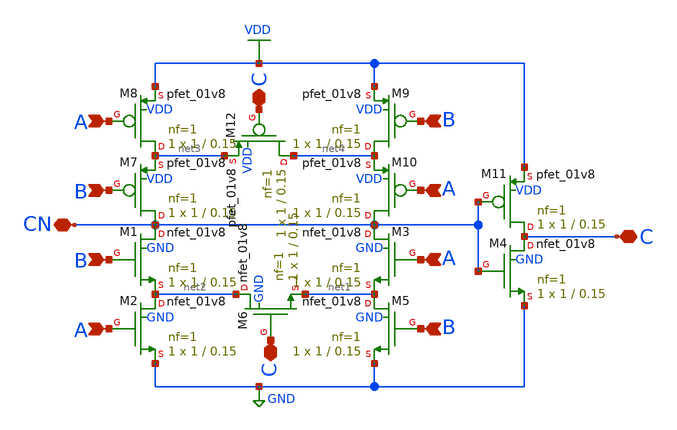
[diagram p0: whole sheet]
** sch_path: cells/xschem/ASYNC3.sch
**.subckt ASYNC3 A B B A B A A B C C CN C
*.ipin A
*.ipin B
*.ipin B
*.ipin A
*.ipin B
*.ipin A
*.ipin A
*.ipin B
*.iopin C
*.iopin C
*.iopin CN
*.iopin C
XM1 CN B net2 GND sky130_fd_pr__nfet_01v8 L=0.15 W=1 nf=1 ad='int((nf+1)/2) * W/nf * 0.29' as='int((nf+2)/2) * W/nf * 0.29'
+ pd='2*int((nf+1)/2) * (W/nf + 0.29)' ps='2*int((nf+2)/2) * (W/nf + 0.29)' nrd='0.29 / W' nrs='0.29 / W'
+ sa=0 sb=0 sd=0 mult=1 m=1
XM2 net2 A GND GND sky130_fd_pr__nfet_01v8 L=0.15 W=1 nf=1 ad='int((nf+1)/2) * W/nf * 0.29' as='int((nf+2)/2) * W/nf * 0.29'
+ pd='2*int((nf+1)/2) * (W/nf + 0.29)' ps='2*int((nf+2)/2) * (W/nf + 0.29)' nrd='0.29 / W' nrs='0.29 / W'
+ sa=0 sb=0 sd=0 mult=1 m=1
XM3 CN A net1 GND sky130_fd_pr__nfet_01v8 L=0.15 W=1 nf=1 ad='int((nf+1)/2) * W/nf * 0.29' as='int((nf+2)/2) * W/nf * 0.29'
+ pd='2*int((nf+1)/2) * (W/nf + 0.29)' ps='2*int((nf+2)/2) * (W/nf + 0.29)' nrd='0.29 / W' nrs='0.29 / W'
+ sa=0 sb=0 sd=0 mult=1 m=1
XM4 C CN GND GND sky130_fd_pr__nfet_01v8 L=0.15 W=1 nf=1 ad='int((nf+1)/2) * W/nf * 0.29' as='int((nf+2)/2) * W/nf * 0.29'
+ pd='2*int((nf+1)/2) * (W/nf + 0.29)' ps='2*int((nf+2)/2) * (W/nf + 0.29)' nrd='0.29 / W' nrs='0.29 / W'
+ sa=0 sb=0 sd=0 mult=1 m=1
XM5 net1 B GND GND sky130_fd_pr__nfet_01v8 L=0.15 W=1 nf=1 ad='int((nf+1)/2) * W/nf * 0.29' as='int((nf+2)/2) * W/nf * 0.29'
+ pd='2*int((nf+1)/2) * (W/nf + 0.29)' ps='2*int((nf+2)/2) * (W/nf + 0.29)' nrd='0.29 / W' nrs='0.29 / W'
+ sa=0 sb=0 sd=0 mult=1 m=1
XM6 net2 C net1 GND sky130_fd_pr__nfet_01v8 L=0.15 W=1 nf=1 ad='int((nf+1)/2) * W/nf * 0.29' as='int((nf+2)/2) * W/nf * 0.29'
+ pd='2*int((nf+1)/2) * (W/nf + 0.29)' ps='2*int((nf+2)/2) * (W/nf + 0.29)' nrd='0.29 / W' nrs='0.29 / W'
+ sa=0 sb=0 sd=0 mult=1 m=1
XM7 CN B net3 VDD sky130_fd_pr__pfet_01v8 L=0.15 W=1 nf=1 ad='int((nf+1)/2) * W/nf * 0.29' as='int((nf+2)/2) * W/nf * 0.29'
+ pd='2*int((nf+1)/2) * (W/nf + 0.29)' ps='2*int((nf+2)/2) * (W/nf + 0.29)' nrd='0.29 / W' nrs='0.29 / W'
+ sa=0 sb=0 sd=0 mult=1 m=1
XM8 net3 A VDD VDD sky130_fd_pr__pfet_01v8 L=0.15 W=1 nf=1 ad='int((nf+1)/2) * W/nf * 0.29' as='int((nf+2)/2) * W/nf * 0.29'
+ pd='2*int((nf+1)/2) * (W/nf + 0.29)' ps='2*int((nf+2)/2) * (W/nf + 0.29)' nrd='0.29 / W' nrs='0.29 / W'
+ sa=0 sb=0 sd=0 mult=1 m=1
XM9 net4 B VDD VDD sky130_fd_pr__pfet_01v8 L=0.15 W=1 nf=1 ad='int((nf+1)/2) * W/nf * 0.29' as='int((nf+2)/2) * W/nf * 0.29'
+ pd='2*int((nf+1)/2) * (W/nf + 0.29)' ps='2*int((nf+2)/2) * (W/nf + 0.29)' nrd='0.29 / W' nrs='0.29 / W'
+ sa=0 sb=0 sd=0 mult=1 m=1
XM10 CN A net4 VDD sky130_fd_pr__pfet_01v8 L=0.15 W=1 nf=1 ad='int((nf+1)/2) * W/nf * 0.29' as='int((nf+2)/2) * W/nf * 0.29'
+ pd='2*int((nf+1)/2) * (W/nf + 0.29)' ps='2*int((nf+2)/2) * (W/nf + 0.29)' nrd='0.29 / W' nrs='0.29 / W'
+ sa=0 sb=0 sd=0 mult=1 m=1
XM11 C CN VDD VDD sky130_fd_pr__pfet_01v8 L=0.15 W=1 nf=1 ad='int((nf+1)/2) * W/nf * 0.29' as='int((nf+2)/2) * W/nf * 0.29'
+ pd='2*int((nf+1)/2) * (W/nf + 0.29)' ps='2*int((nf+2)/2) * (W/nf + 0.29)' nrd='0.29 / W' nrs='0.29 / W'
+ sa=0 sb=0 sd=0 mult=1 m=1
XM12 net4 C net3 VDD sky130_fd_pr__pfet_01v8 L=0.15 W=1 nf=1 ad='int((nf+1)/2) * W/nf * 0.29' as='int((nf+2)/2) * W/nf * 0.29'
+ pd='2*int((nf+1)/2) * (W/nf + 0.29)' ps='2*int((nf+2)/2) * (W/nf + 0.29)' nrd='0.29 / W' nrs='0.29 / W'
+ sa=0 sb=0 sd=0 mult=1 m=1
**.ends
.GLOBAL VDD
.GLOBAL GND
.end
